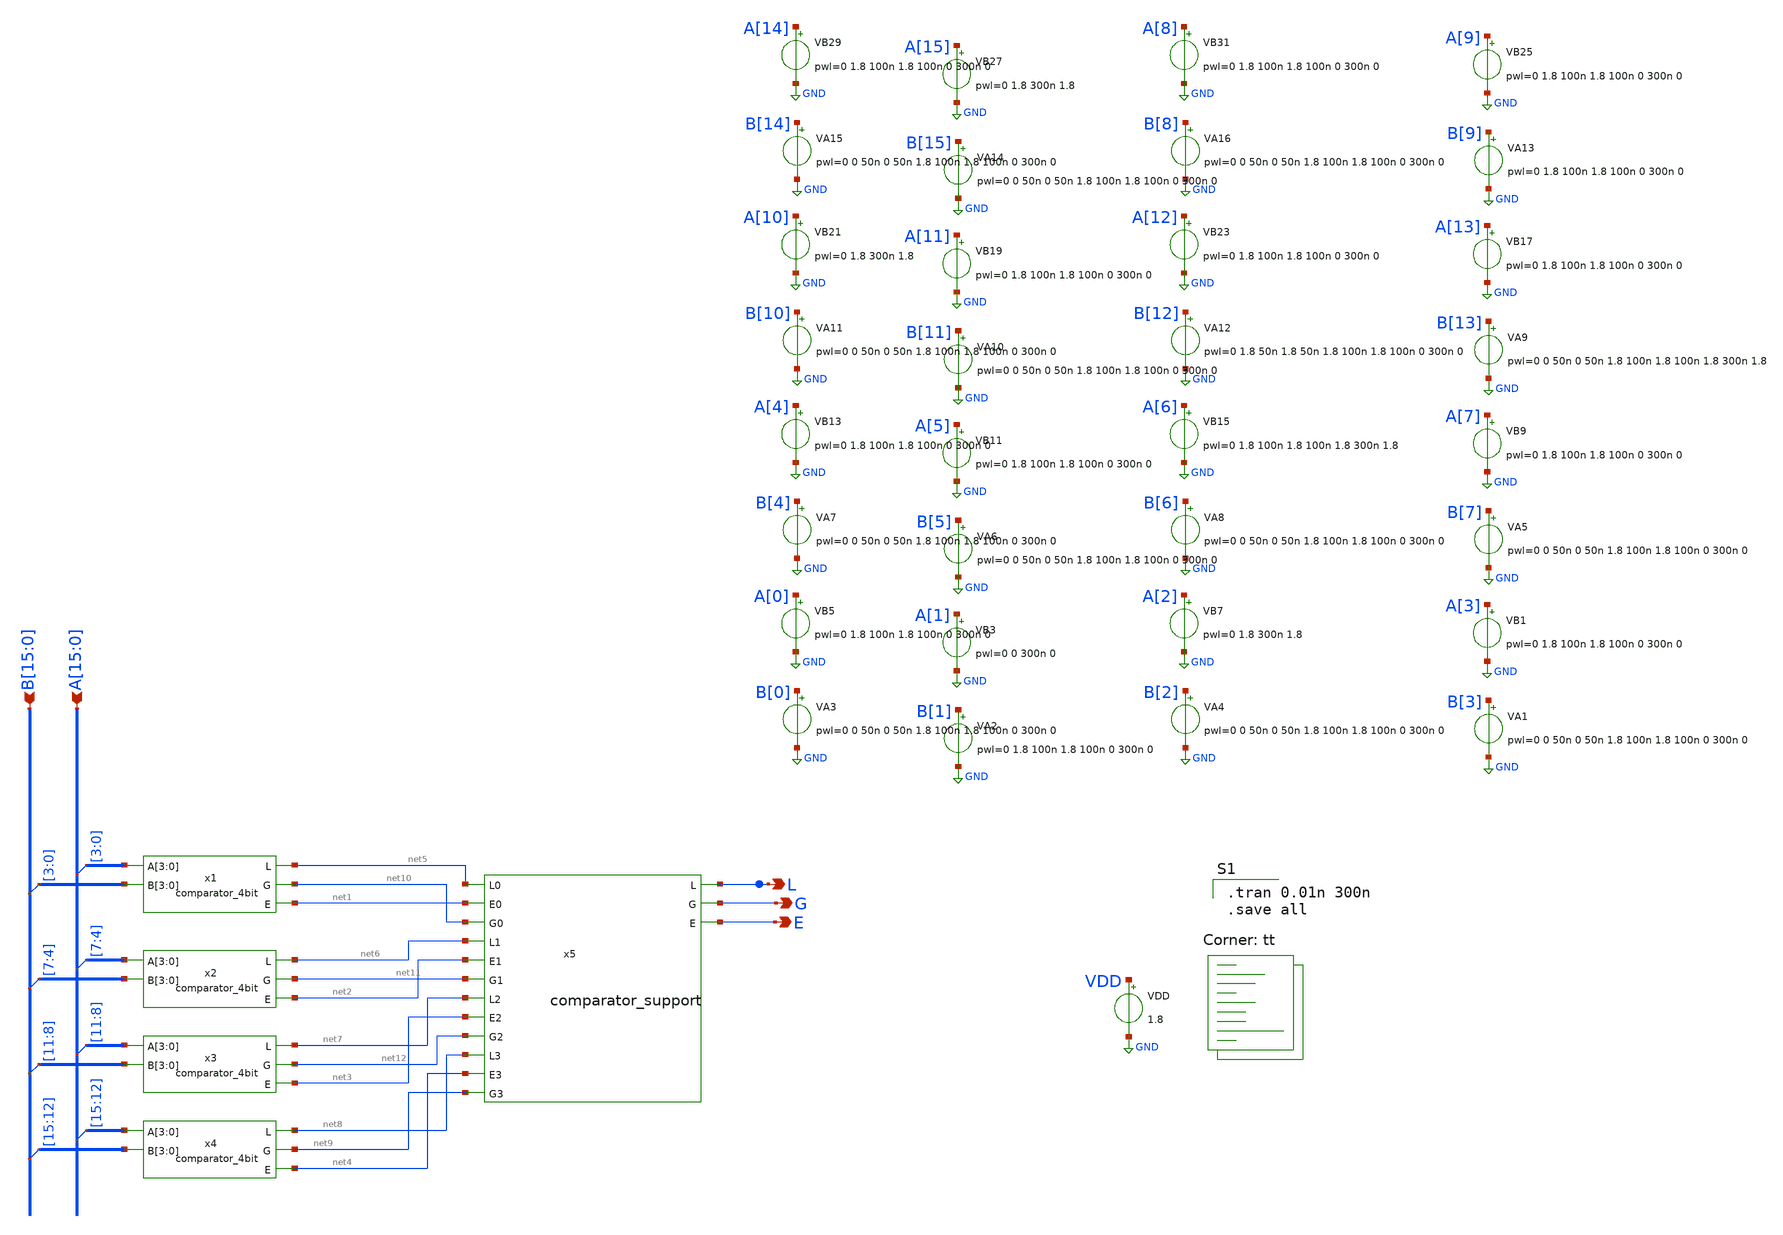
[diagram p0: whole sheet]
** sch_path: gates/16 bit comparatorsim.sch
**.subckt 16 bit comparatorsim
*+ A[15],A[14],A[13],A[12],A[11],A[10],A[9],A[8],A[7],A[6],A[5],A[4],A[3],A[2],A[1],A[0] B[15],B[14],B[13],B[12],B[11],B[10],B[9],B[8],B[7],B[6],B[5],B[4],B[3],B[2],B[1],B[0] L G E
*.ipin A[15],A[14],A[13],A[12],A[11],A[10],A[9],A[8],A[7],A[6],A[5],A[4],A[3],A[2],A[1],A[0]
*.ipin B[15],B[14],B[13],B[12],B[11],B[10],B[9],B[8],B[7],B[6],B[5],B[4],B[3],B[2],B[1],B[0]
*.opin L
*.opin G
*.opin E
x1 A[3] A[2] A[1] A[0] B[3] B[2] B[1] B[0] net5 net10 net1 comparator_4bit
x2 A[7] A[6] A[5] A[4] B[7] B[6] B[5] B[4] net6 net11 net2 comparator_4bit
x3 A[11] A[10] A[9] A[8] B[11] B[10] B[9] B[8] net7 net12 net3 comparator_4bit
x4 A[15] A[14] A[13] A[12] B[15] B[14] B[13] B[12] net8 net9 net4 comparator_4bit
* tap: A[15:0] --> A[3:0]
* tap: A[15:0] --> A[7:4]
* tap: A[15:0] --> A[15:12]
* tap: A[15:0] --> A[11:8]
* tap: B[15:0] --> B[15:12]
* tap: B[15:0] --> B[11:8]
* tap: B[15:0] --> B[7:4]
* tap: B[15:0] --> B[3:0]
VDD VDD GND 1.8
VA1 B[3] GND pwl=0 0 50n 0 50n 1.8 100n 1.8 100n 0 300n 0
VB1 A[3] GND pwl=0 1.8 100n 1.8 100n 0 300n 0
VA2 B[1] GND pwl=0 1.8 100n 1.8 100n 0 300n 0
VB3 A[1] GND pwl=0 0 300n 0
VA3 B[0] GND pwl=0 0 50n 0 50n 1.8 100n 1.8 100n 0 300n 0
VB5 A[0] GND pwl=0 1.8 100n 1.8 100n 0 300n 0
VA4 B[2] GND pwl=0 0 50n 0 50n 1.8 100n 1.8 100n 0 300n 0
VB7 A[2] GND pwl=0 1.8 300n 1.8
VA5 B[7] GND pwl=0 0 50n 0 50n 1.8 100n 1.8 100n 0 300n 0
VB9 A[7] GND pwl=0 1.8 100n 1.8 100n 0 300n 0
VA6 B[5] GND pwl=0 0 50n 0 50n 1.8 100n 1.8 100n 0 300n 0
VB11 A[5] GND pwl=0 1.8 100n 1.8 100n 0 300n 0
VA7 B[4] GND pwl=0 0 50n 0 50n 1.8 100n 1.8 100n 0 300n 0
VB13 A[4] GND pwl=0 1.8 100n 1.8 100n 0 300n 0
VA8 B[6] GND pwl=0 0 50n 0 50n 1.8 100n 1.8 100n 0 300n 0
VB15 A[6] GND pwl=0 1.8 100n 1.8 100n 1.8 300n 1.8
VA9 B[13] GND pwl=0 0 50n 0 50n 1.8 100n 1.8 100n 1.8 300n 1.8
VB17 A[13] GND pwl=0 1.8 100n 1.8 100n 0 300n 0
VA10 B[11] GND pwl=0 0 50n 0 50n 1.8 100n 1.8 100n 0 300n 0
VB19 A[11] GND pwl=0 1.8 100n 1.8 100n 0 300n 0
VA11 B[10] GND pwl=0 0 50n 0 50n 1.8 100n 1.8 100n 0 300n 0
VB21 A[10] GND pwl=0 1.8 300n 1.8
VA12 B[12] GND pwl=0 1.8 50n 1.8 50n 1.8 100n 1.8 100n 0 300n 0
VB23 A[12] GND pwl=0 1.8 100n 1.8 100n 0 300n 0
VA13 B[9] GND pwl=0 1.8 100n 1.8 100n 0 300n 0
VB25 A[9] GND pwl=0 1.8 100n 1.8 100n 0 300n 0
VA14 B[15] GND pwl=0 0 50n 0 50n 1.8 100n 1.8 100n 0 300n 0
VB27 A[15] GND pwl=0 1.8 300n 1.8
VA15 B[14] GND pwl=0 0 50n 0 50n 1.8 100n 1.8 100n 0 300n 0
VB29 A[14] GND pwl=0 1.8 100n 1.8 100n 0 300n 0
VA16 B[8] GND pwl=0 0 50n 0 50n 1.8 100n 1.8 100n 0 300n 0
VB31 A[8] GND pwl=0 1.8 100n 1.8 100n 0 300n 0
x5 net5 net1 net10 net6 net2 L net11 net7 G net3 net12 net8 net4 E net9 comparator_support
**** begin user architecture code

.tran 0.01n 300n
.save all

.lib $::SKYWATER_MODELS/sky130.lib.spice tt
**** end user architecture code
**.ends

* expanding   symbol:  comparator_4bit.sym # of pins=5
** sym_path: gates/comparator_4bit.sym
** sch_path: gates/comparator_4bit.sch
.subckt comparator_4bit A[3] A[2] A[1] A[0] B[3] B[2] B[1] B[0] L G E
*.opin L
*.opin G
*.opin E
*.ipin A[3],A[2],A[1],A[0]
*.ipin B[3],B[2],B[1],B[0]
x5 net2 net3 net4 AND2
x6 net2 net9 net5 AND2
x7 net2 net8 net7 AND2
x8 net13 E net17 AND2
x9 net13 net14 net16 AND2
x10 net13 net15 net18 AND2
x11 net9 net13 net10 AND2
x12 net9 net19 net11 AND2
x13 net9 net20 net12 AND2
x14 net1 net3 net19 L net14 OR4
x15 net6 net8 net20 G net15 OR4
X1 A[0] net21 inv_vtc
X2 B[0] net22 inv_vtc
x3 net21 net1 B[0] AND2
x16 A[0] net6 net22 AND2
x17 net1 net2 net6 NOR2
X18 A[1] net23 inv_vtc
X19 B[1] net24 inv_vtc
x20 net23 net4 B[1] AND2
x21 A[1] net7 net24 AND2
x22 net4 net5 net7 NOR2
X23 A[2] net25 inv_vtc
X24 B[2] net26 inv_vtc
x25 net25 net11 B[2] AND2
x26 A[2] net12 net26 AND2
x27 net11 net10 net12 NOR2
X28 A[3] net27 inv_vtc
X29 B[3] net28 inv_vtc
x30 net27 net16 B[3] AND2
x31 A[3] net18 net28 AND2
x32 net16 net17 net18 NOR2
* tap: A[3:0] --> A[0]
* tap: A[3:0] --> A[1]
* tap: A[3:0] --> A[2]
* tap: A[3:0] --> A[3]
* tap: B[3:0] --> B[0]
* tap: B[3:0] --> B[1]
* tap: B[3:0] --> B[2]
* tap: B[3:0] --> B[3]
.ends


* expanding   symbol:  comparator_support.sym # of pins=15
** sym_path: gates/comparator_support.sym
** sch_path: gates/comparator_support.sch
.subckt comparator_support L0 E0 G0 L1 E1 L G1 L2 G E2 G2 L3 E3 E G3
*.opin L
*.opin G
*.opin E
*.ipin L0
*.ipin E0
*.ipin G0
*.ipin G1
*.ipin G2
*.ipin G3
*.ipin E1
*.ipin E2
*.ipin E3
*.ipin L1
*.ipin L2
*.ipin L3
x5 E0 net1 L1 AND2
x6 E0 net3 E1 AND2
x7 E0 net2 G1 AND2
x8 net4 E E3 AND2
x9 net4 net5 L3 AND2
x10 net4 net6 G3 AND2
x11 net3 net4 E2 AND2
x12 net3 net7 L2 AND2
x13 net3 net8 G2 AND2
x14 L0 net1 net7 L net5 OR4
x15 G0 net2 net8 G net6 OR4
.ends


* expanding   symbol:  AND2.sym # of pins=3
** sym_path: gates/AND2.sym
** sch_path: gates/AND2.sch
.subckt AND2 A Y B
*.opin Y
*.ipin A
*.ipin B
x1 A net1 B NAND2_Gate
X2 net1 Y inv_vtc
.ends


* expanding   symbol:  OR4.sym # of pins=5
** sym_path: gates/OR4.sym
** sch_path: gates/OR4.sch
.subckt OR4 D C B Y A
*.ipin A
*.ipin B
*.opin Y
*.ipin C
*.ipin D
XM2 GND D net1 GND sky130_fd_pr__nfet_01v8 L=0.15 W=1 nf=1 ad='int((nf+1)/2) * W/nf * 0.29' as='int((nf+2)/2) * W/nf * 0.29'
+ pd='2*int((nf+1)/2) * (W/nf + 0.29)' ps='2*int((nf+2)/2) * (W/nf + 0.29)' nrd='0.29 / W' nrs='0.29 / W'
+ sa=0 sb=0 sd=0 mult=1 m=1
XM4 VDD D net4 VDD sky130_fd_pr__pfet_01v8 L=0.15 W=1 nf=1 ad='int((nf+1)/2) * W/nf * 0.29' as='int((nf+2)/2) * W/nf * 0.29'
+ pd='2*int((nf+1)/2) * (W/nf + 0.29)' ps='2*int((nf+2)/2) * (W/nf + 0.29)' nrd='0.29 / W' nrs='0.29 / W'
+ sa=0 sb=0 sd=0 mult=1 m=1
XM5 net4 C net3 VDD sky130_fd_pr__pfet_01v8 L=0.15 W=1 nf=1 ad='int((nf+1)/2) * W/nf * 0.29' as='int((nf+2)/2) * W/nf * 0.29'
+ pd='2*int((nf+1)/2) * (W/nf + 0.29)' ps='2*int((nf+2)/2) * (W/nf + 0.29)' nrd='0.29 / W' nrs='0.29 / W'
+ sa=0 sb=0 sd=0 mult=1 m=1
XM6 GND C net1 GND sky130_fd_pr__nfet_01v8 L=0.15 W=1 nf=1 ad='int((nf+1)/2) * W/nf * 0.29' as='int((nf+2)/2) * W/nf * 0.29'
+ pd='2*int((nf+1)/2) * (W/nf + 0.29)' ps='2*int((nf+2)/2) * (W/nf + 0.29)' nrd='0.29 / W' nrs='0.29 / W'
+ sa=0 sb=0 sd=0 mult=1 m=1
XM7 net3 B net2 VDD sky130_fd_pr__pfet_01v8 L=0.15 W=1 nf=1 ad='int((nf+1)/2) * W/nf * 0.29' as='int((nf+2)/2) * W/nf * 0.29'
+ pd='2*int((nf+1)/2) * (W/nf + 0.29)' ps='2*int((nf+2)/2) * (W/nf + 0.29)' nrd='0.29 / W' nrs='0.29 / W'
+ sa=0 sb=0 sd=0 mult=1 m=1
XM8 GND B net1 GND sky130_fd_pr__nfet_01v8 L=0.15 W=1 nf=1 ad='int((nf+1)/2) * W/nf * 0.29' as='int((nf+2)/2) * W/nf * 0.29'
+ pd='2*int((nf+1)/2) * (W/nf + 0.29)' ps='2*int((nf+2)/2) * (W/nf + 0.29)' nrd='0.29 / W' nrs='0.29 / W'
+ sa=0 sb=0 sd=0 mult=1 m=1
XM9 net2 A net1 VDD sky130_fd_pr__pfet_01v8 L=0.15 W=1 nf=1 ad='int((nf+1)/2) * W/nf * 0.29' as='int((nf+2)/2) * W/nf * 0.29'
+ pd='2*int((nf+1)/2) * (W/nf + 0.29)' ps='2*int((nf+2)/2) * (W/nf + 0.29)' nrd='0.29 / W' nrs='0.29 / W'
+ sa=0 sb=0 sd=0 mult=1 m=1
XM10 GND A net1 GND sky130_fd_pr__nfet_01v8 L=0.15 W=1 nf=1 ad='int((nf+1)/2) * W/nf * 0.29' as='int((nf+2)/2) * W/nf * 0.29'
+ pd='2*int((nf+1)/2) * (W/nf + 0.29)' ps='2*int((nf+2)/2) * (W/nf + 0.29)' nrd='0.29 / W' nrs='0.29 / W'
+ sa=0 sb=0 sd=0 mult=1 m=1
X2 net1 Y inv_vtc
.ends


* expanding   symbol:  /home/apn/test_xschem_sky130/inv_vtc.sym # of pins=2
** sym_path: gates/inv_vtc.sym
** sch_path: gates/inv_vtc.sch
.subckt inv_vtc A Y
*.ipin A
*.opin Y
XM1 Y A VDD VDD sky130_fd_pr__pfet_01v8 L=0.15 W=2 nf=1 ad='int((nf+1)/2) * W/nf * 0.29' as='int((nf+2)/2) * W/nf * 0.29'
+ pd='2*int((nf+1)/2) * (W/nf + 0.29)' ps='2*int((nf+2)/2) * (W/nf + 0.29)' nrd='0.29 / W' nrs='0.29 / W'
+ sa=0 sb=0 sd=0 mult=1 m=1
XM2 Y A GND GND sky130_fd_pr__nfet_01v8 L=0.15 W=1 nf=1 ad='int((nf+1)/2) * W/nf * 0.29' as='int((nf+2)/2) * W/nf * 0.29'
+ pd='2*int((nf+1)/2) * (W/nf + 0.29)' ps='2*int((nf+2)/2) * (W/nf + 0.29)' nrd='0.29 / W' nrs='0.29 / W'
+ sa=0 sb=0 sd=0 mult=1 m=1
.ends


* expanding   symbol:  NOR2.sym # of pins=3
** sym_path: gates/NOR2.sym
** sch_path: gates/NOR2.sch
.subckt NOR2 B Y A
*.ipin A
*.ipin B
*.opin Y
XM7 VDD B net1 VDD sky130_fd_pr__pfet_01v8 L=0.15 W=1 nf=1 ad='int((nf+1)/2) * W/nf * 0.29' as='int((nf+2)/2) * W/nf * 0.29'
+ pd='2*int((nf+1)/2) * (W/nf + 0.29)' ps='2*int((nf+2)/2) * (W/nf + 0.29)' nrd='0.29 / W' nrs='0.29 / W'
+ sa=0 sb=0 sd=0 mult=1 m=1
XM8 GND B Y GND sky130_fd_pr__nfet_01v8 L=0.15 W=1 nf=1 ad='int((nf+1)/2) * W/nf * 0.29' as='int((nf+2)/2) * W/nf * 0.29'
+ pd='2*int((nf+1)/2) * (W/nf + 0.29)' ps='2*int((nf+2)/2) * (W/nf + 0.29)' nrd='0.29 / W' nrs='0.29 / W'
+ sa=0 sb=0 sd=0 mult=1 m=1
XM9 net1 A Y VDD sky130_fd_pr__pfet_01v8 L=0.15 W=1 nf=1 ad='int((nf+1)/2) * W/nf * 0.29' as='int((nf+2)/2) * W/nf * 0.29'
+ pd='2*int((nf+1)/2) * (W/nf + 0.29)' ps='2*int((nf+2)/2) * (W/nf + 0.29)' nrd='0.29 / W' nrs='0.29 / W'
+ sa=0 sb=0 sd=0 mult=1 m=1
XM10 GND A Y GND sky130_fd_pr__nfet_01v8 L=0.15 W=1 nf=1 ad='int((nf+1)/2) * W/nf * 0.29' as='int((nf+2)/2) * W/nf * 0.29'
+ pd='2*int((nf+1)/2) * (W/nf + 0.29)' ps='2*int((nf+2)/2) * (W/nf + 0.29)' nrd='0.29 / W' nrs='0.29 / W'
+ sa=0 sb=0 sd=0 mult=1 m=1
.ends


* expanding   symbol:  NAND2_Gate.sym # of pins=3
** sym_path: gates/NAND2_Gate.sym
** sch_path: gates/NAND2_Gate.sch
.subckt NAND2_Gate A Y B
*.ipin A
*.ipin B
*.opin Y
XM1 Y A net1 GND sky130_fd_pr__nfet_01v8 L=0.15 W=1 nf=1 ad='int((nf+1)/2) * W/nf * 0.29' as='int((nf+2)/2) * W/nf * 0.29'
+ pd='2*int((nf+1)/2) * (W/nf + 0.29)' ps='2*int((nf+2)/2) * (W/nf + 0.29)' nrd='0.29 / W' nrs='0.29 / W'
+ sa=0 sb=0 sd=0 mult=1 m=1
XM2 net1 B GND GND sky130_fd_pr__nfet_01v8 L=0.15 W=1 nf=1 ad='int((nf+1)/2) * W/nf * 0.29' as='int((nf+2)/2) * W/nf * 0.29'
+ pd='2*int((nf+1)/2) * (W/nf + 0.29)' ps='2*int((nf+2)/2) * (W/nf + 0.29)' nrd='0.29 / W' nrs='0.29 / W'
+ sa=0 sb=0 sd=0 mult=1 m=1
XM3 Y A VDD VDD sky130_fd_pr__pfet_01v8 L=0.15 W=1 nf=1 ad='int((nf+1)/2) * W/nf * 0.29' as='int((nf+2)/2) * W/nf * 0.29'
+ pd='2*int((nf+1)/2) * (W/nf + 0.29)' ps='2*int((nf+2)/2) * (W/nf + 0.29)' nrd='0.29 / W' nrs='0.29 / W'
+ sa=0 sb=0 sd=0 mult=1 m=1
XM4 Y B VDD VDD sky130_fd_pr__pfet_01v8 L=0.15 W=1 nf=1 ad='int((nf+1)/2) * W/nf * 0.29' as='int((nf+2)/2) * W/nf * 0.29'
+ pd='2*int((nf+1)/2) * (W/nf + 0.29)' ps='2*int((nf+2)/2) * (W/nf + 0.29)' nrd='0.29 / W' nrs='0.29 / W'
+ sa=0 sb=0 sd=0 mult=1 m=1
.ends

.GLOBAL GND
.GLOBAL VDD
.end
